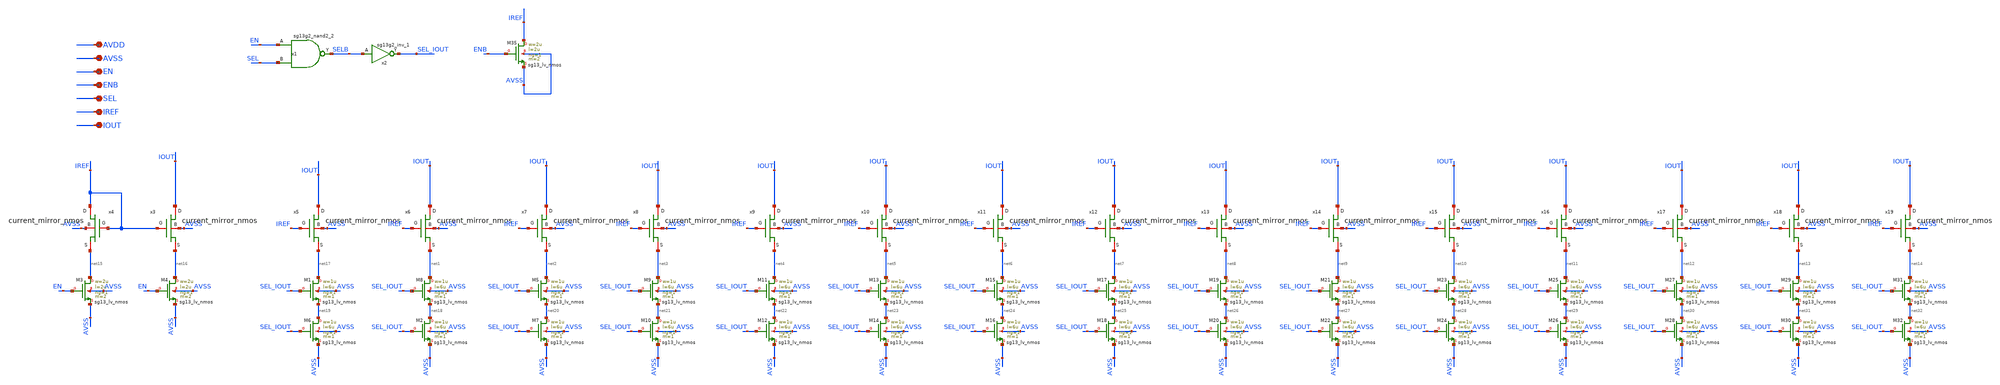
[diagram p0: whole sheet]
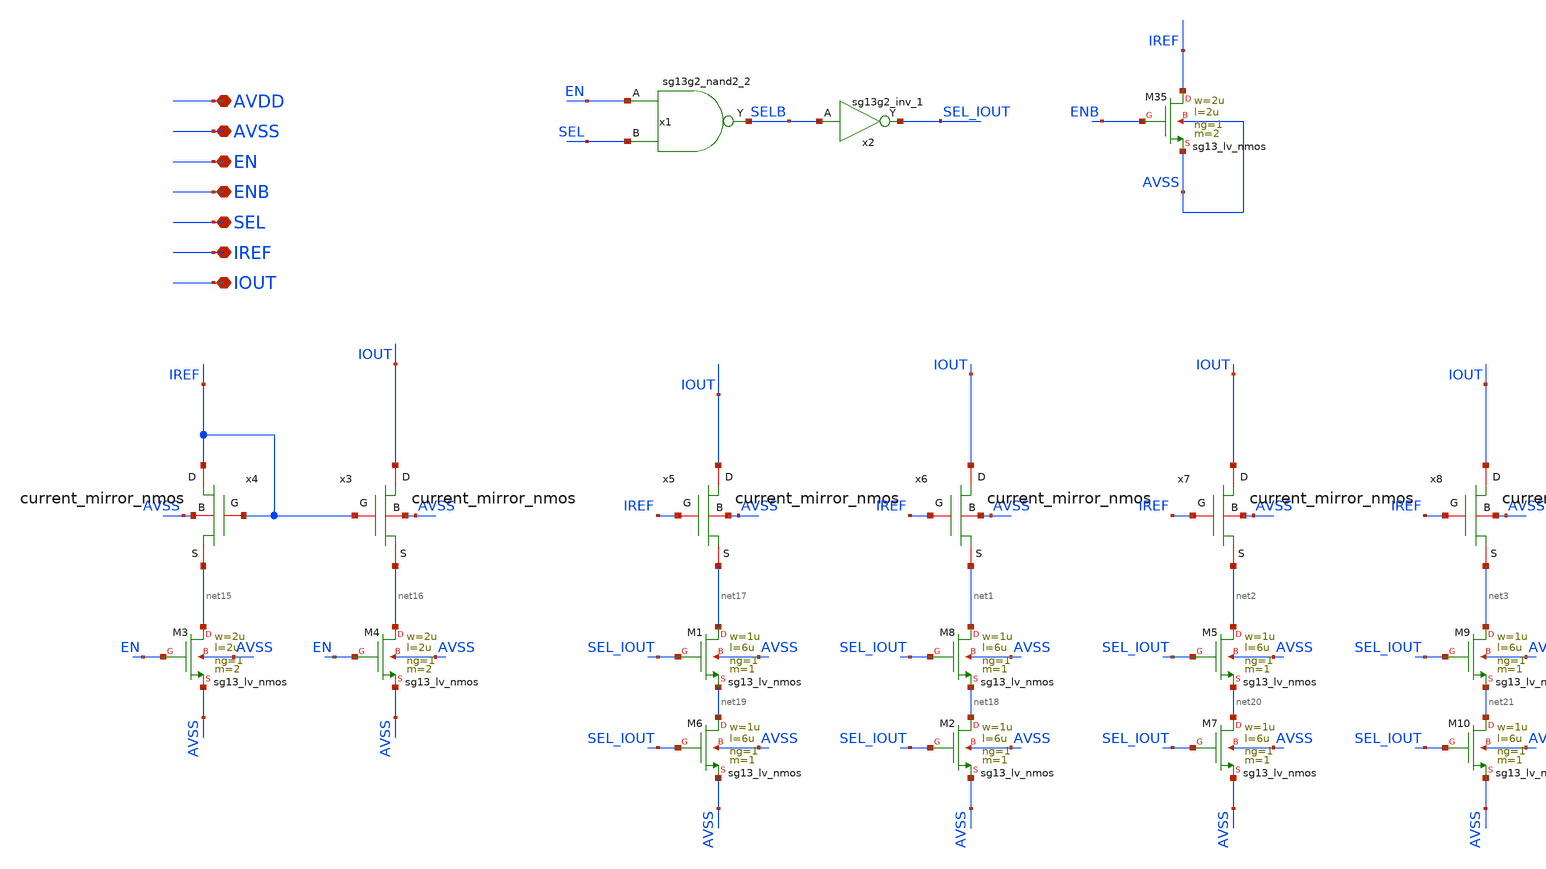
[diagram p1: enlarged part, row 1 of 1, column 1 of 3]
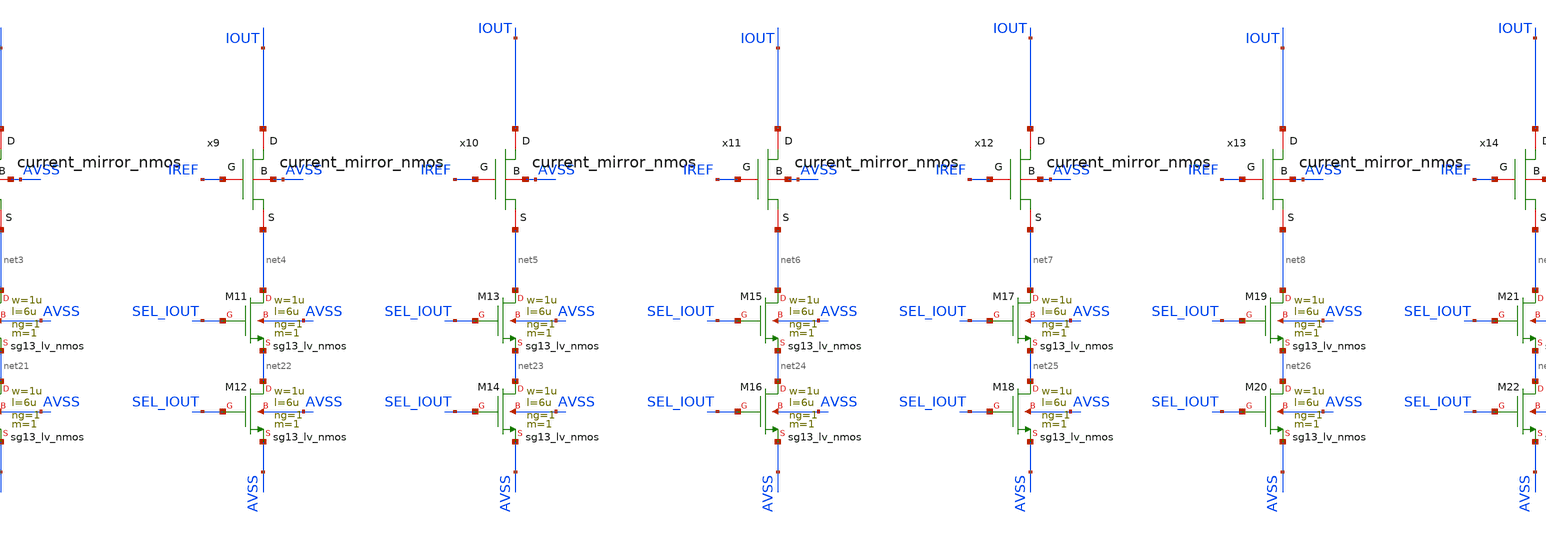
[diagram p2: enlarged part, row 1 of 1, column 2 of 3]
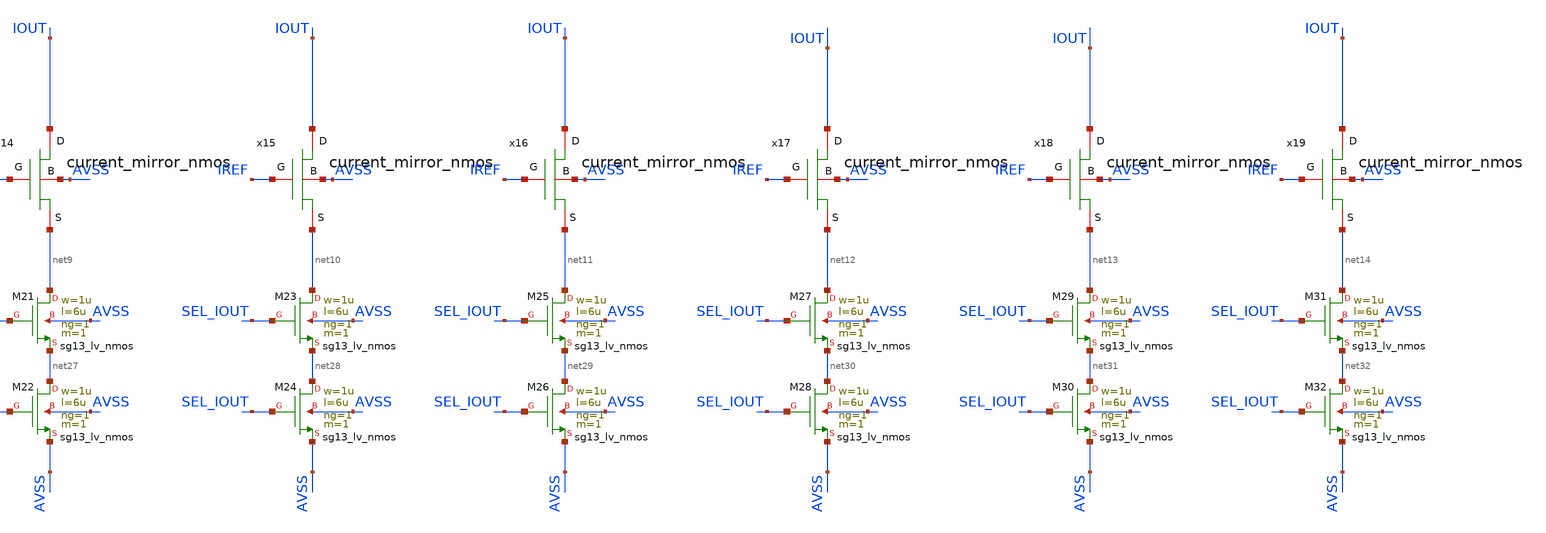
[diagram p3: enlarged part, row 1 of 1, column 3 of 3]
** sch_path: DAC/current_mirror.sch
**.subckt current_mirror AVDD AVSS EN ENB SEL IREF IOUT
*.iopin AVDD
*.iopin AVSS
*.iopin EN
*.iopin ENB
*.iopin SEL
*.iopin IREF
*.iopin IOUT
XM3 net15 EN AVSS AVSS sg13_lv_nmos w=2u l=2u ng=1 m=2 mm_ok=1
XM4 net16 EN AVSS AVSS sg13_lv_nmos w=2u l=2u ng=1 m=2 mm_ok=1
XM8 net1 SEL_IOUT net18 AVSS sg13_lv_nmos w=1u l=6u ng=1 m=1 mm_ok=1
x1 SELB EN SEL AVDD AVSS sg13g2_nand2_2
x2 SEL_IOUT SELB AVDD AVSS sg13g2_inv_1
XM35 IREF ENB AVSS AVSS sg13_lv_nmos w=2u l=2u ng=1 m=2 mm_ok=1
x3 IOUT net16 IREF AVSS current_mirror_nmos
x4 IREF net15 IREF AVSS current_mirror_nmos
x5 IOUT net17 IREF AVSS current_mirror_nmos
x6 IOUT net1 IREF AVSS current_mirror_nmos
x7 IOUT net2 IREF AVSS current_mirror_nmos
x8 IOUT net3 IREF AVSS current_mirror_nmos
x9 IOUT net4 IREF AVSS current_mirror_nmos
x10 IOUT net5 IREF AVSS current_mirror_nmos
x11 IOUT net6 IREF AVSS current_mirror_nmos
x12 IOUT net7 IREF AVSS current_mirror_nmos
x13 IOUT net8 IREF AVSS current_mirror_nmos
x14 IOUT net9 IREF AVSS current_mirror_nmos
x15 IOUT net10 IREF AVSS current_mirror_nmos
x16 IOUT net11 IREF AVSS current_mirror_nmos
x17 IOUT net12 IREF AVSS current_mirror_nmos
x18 IOUT net13 IREF AVSS current_mirror_nmos
x19 IOUT net14 IREF AVSS current_mirror_nmos
XM2 net18 SEL_IOUT AVSS AVSS sg13_lv_nmos w=1u l=6u ng=1 m=1 mm_ok=1
XM1 net17 SEL_IOUT net19 AVSS sg13_lv_nmos w=1u l=6u ng=1 m=1 mm_ok=1
XM6 net19 SEL_IOUT AVSS AVSS sg13_lv_nmos w=1u l=6u ng=1 m=1 mm_ok=1
XM5 net2 SEL_IOUT net20 AVSS sg13_lv_nmos w=1u l=6u ng=1 m=1 mm_ok=1
XM7 net20 SEL_IOUT AVSS AVSS sg13_lv_nmos w=1u l=6u ng=1 m=1 mm_ok=1
XM9 net3 SEL_IOUT net21 AVSS sg13_lv_nmos w=1u l=6u ng=1 m=1 mm_ok=1
XM10 net21 SEL_IOUT AVSS AVSS sg13_lv_nmos w=1u l=6u ng=1 m=1 mm_ok=1
XM11 net4 SEL_IOUT net22 AVSS sg13_lv_nmos w=1u l=6u ng=1 m=1 mm_ok=1
XM12 net22 SEL_IOUT AVSS AVSS sg13_lv_nmos w=1u l=6u ng=1 m=1 mm_ok=1
XM13 net5 SEL_IOUT net23 AVSS sg13_lv_nmos w=1u l=6u ng=1 m=1 mm_ok=1
XM14 net23 SEL_IOUT AVSS AVSS sg13_lv_nmos w=1u l=6u ng=1 m=1 mm_ok=1
XM15 net6 SEL_IOUT net24 AVSS sg13_lv_nmos w=1u l=6u ng=1 m=1 mm_ok=1
XM16 net24 SEL_IOUT AVSS AVSS sg13_lv_nmos w=1u l=6u ng=1 m=1 mm_ok=1
XM17 net7 SEL_IOUT net25 AVSS sg13_lv_nmos w=1u l=6u ng=1 m=1 mm_ok=1
XM18 net25 SEL_IOUT AVSS AVSS sg13_lv_nmos w=1u l=6u ng=1 m=1 mm_ok=1
XM19 net8 SEL_IOUT net26 AVSS sg13_lv_nmos w=1u l=6u ng=1 m=1 mm_ok=1
XM20 net26 SEL_IOUT AVSS AVSS sg13_lv_nmos w=1u l=6u ng=1 m=1 mm_ok=1
XM21 net9 SEL_IOUT net27 AVSS sg13_lv_nmos w=1u l=6u ng=1 m=1 mm_ok=1
XM22 net27 SEL_IOUT AVSS AVSS sg13_lv_nmos w=1u l=6u ng=1 m=1 mm_ok=1
XM23 net10 SEL_IOUT net28 AVSS sg13_lv_nmos w=1u l=6u ng=1 m=1 mm_ok=1
XM24 net28 SEL_IOUT AVSS AVSS sg13_lv_nmos w=1u l=6u ng=1 m=1 mm_ok=1
XM25 net11 SEL_IOUT net29 AVSS sg13_lv_nmos w=1u l=6u ng=1 m=1 mm_ok=1
XM26 net29 SEL_IOUT AVSS AVSS sg13_lv_nmos w=1u l=6u ng=1 m=1 mm_ok=1
XM27 net12 SEL_IOUT net30 AVSS sg13_lv_nmos w=1u l=6u ng=1 m=1 mm_ok=1
XM28 net30 SEL_IOUT AVSS AVSS sg13_lv_nmos w=1u l=6u ng=1 m=1 mm_ok=1
XM29 net13 SEL_IOUT net31 AVSS sg13_lv_nmos w=1u l=6u ng=1 m=1 mm_ok=1
XM30 net31 SEL_IOUT AVSS AVSS sg13_lv_nmos w=1u l=6u ng=1 m=1 mm_ok=1
XM31 net14 SEL_IOUT net32 AVSS sg13_lv_nmos w=1u l=6u ng=1 m=1 mm_ok=1
XM32 net32 SEL_IOUT AVSS AVSS sg13_lv_nmos w=1u l=6u ng=1 m=1 mm_ok=1
**.ends
.end
